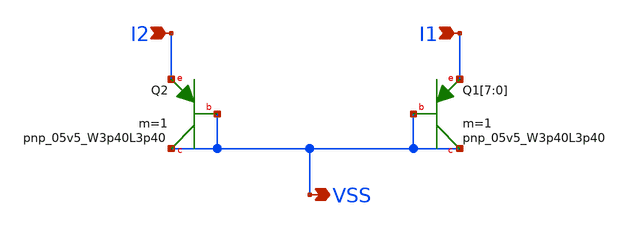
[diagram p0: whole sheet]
** sch_path: design/LELO_GR01_SKY130A/Diodes.sch
**.subckt Diodes VSS I2 I1
*.opin VSS
*.ipin I2
*.ipin I1
XQ1[7] VSS VSS I1 sky130_fd_pr__pnp_05v5_W3p40L3p40 m=1
XQ1[6] VSS VSS I1 sky130_fd_pr__pnp_05v5_W3p40L3p40 m=1
XQ1[5] VSS VSS I1 sky130_fd_pr__pnp_05v5_W3p40L3p40 m=1
XQ1[4] VSS VSS I1 sky130_fd_pr__pnp_05v5_W3p40L3p40 m=1
XQ1[3] VSS VSS I1 sky130_fd_pr__pnp_05v5_W3p40L3p40 m=1
XQ1[2] VSS VSS I1 sky130_fd_pr__pnp_05v5_W3p40L3p40 m=1
XQ1[1] VSS VSS I1 sky130_fd_pr__pnp_05v5_W3p40L3p40 m=1
XQ1[0] VSS VSS I1 sky130_fd_pr__pnp_05v5_W3p40L3p40 m=1
XQ2 VSS VSS I2 sky130_fd_pr__pnp_05v5_W3p40L3p40 m=1
**.ends
.end
